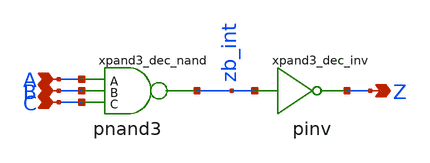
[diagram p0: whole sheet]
** sch_path: sram_4_16_scn4m/and3_dec.sch
**.subckt and3_dec A B C Z
*.ipin A
*.ipin B
*.ipin C
*.opin Z
xpand3_dec_nand A B C zb_int vdd gnd pnand3
xpand3_dec_inv zb_int Z vdd gnd pinv
**.ends
.end
